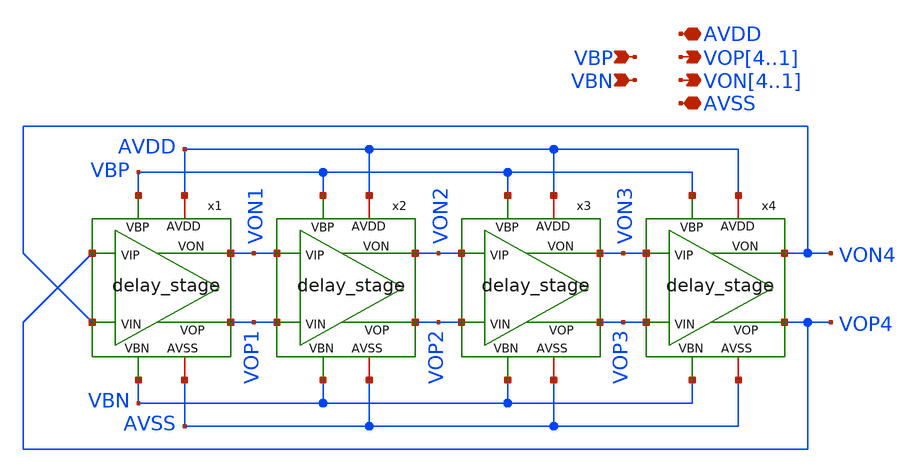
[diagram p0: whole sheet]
** sch_path: designs/libs/core_analog/vco/vco.sch
**.subckt vco VOP4,VOP3,VOP2,VOP1 VON4,VON3,VON2,VON1 VBP VBN AVDD AVSS
*.opin VOP4,VOP3,VOP2,VOP1
*.opin VON4,VON3,VON2,VON1
*.ipin VBP
*.ipin VBN
*.iopin AVDD
*.iopin AVSS
x1 VOP1 AVDD VOP4 VON4 VON1 AVSS VBP VBN delay_stage
x2 VOP2 AVDD VON1 VOP1 VON2 AVSS VBP VBN delay_stage
x3 VOP3 AVDD VON2 VOP2 VON3 AVSS VBP VBN delay_stage
x4 VOP4 AVDD VON3 VOP3 VON4 AVSS VBP VBN delay_stage
**.ends

* expanding   symbol:  libs/core_analog/delay_stage/delay_stage.sym # of pins=8
** sym_path: designs/libs/core_analog/delay_stage/delay_stage.sym
** sch_path: designs/libs/core_analog/delay_stage/delay_stage.sch
.subckt delay_stage VOP AVDD VIP VIN VON AVSS VBP VBN
*.ipin VIP
*.ipin VIN
*.opin VOP
*.opin VON
*.iopin AVDD
*.iopin AVSS
*.ipin VBP
*.ipin VBN
XM5 VON VIP net1 AVSS nfet_03v3 L=0.5u W=2.08u nf=1 ad='int((nf+1)/2) * W/nf * 0.18u' as='int((nf+2)/2) * W/nf * 0.18u'
+ pd='2*int((nf+1)/2) * (W/nf + 0.18u)' ps='2*int((nf+2)/2) * (W/nf + 0.18u)' nrd='0.18u / W' nrs='0.18u / W'
+ sa=0 sb=0 sd=0 m=8
XM2 VON VON AVDD AVDD pfet_03v3 L=1.5u W=1.1u nf=1 ad='int((nf+1)/2) * W/nf * 0.18u' as='int((nf+2)/2) * W/nf * 0.18u'
+ pd='2*int((nf+1)/2) * (W/nf + 0.18u)' ps='2*int((nf+2)/2) * (W/nf + 0.18u)' nrd='0.18u / W' nrs='0.18u / W'
+ sa=0 sb=0 sd=0 m=8
XM6 VOP VIN net1 AVSS nfet_03v3 L=0.5u W=2.08u nf=1 ad='int((nf+1)/2) * W/nf * 0.18u' as='int((nf+2)/2) * W/nf * 0.18u'
+ pd='2*int((nf+1)/2) * (W/nf + 0.18u)' ps='2*int((nf+2)/2) * (W/nf + 0.18u)' nrd='0.18u / W' nrs='0.18u / W'
+ sa=0 sb=0 sd=0 m=8
XM1 VON VBP AVDD AVDD pfet_03v3 L=1.5u W=1.1u nf=1 ad='int((nf+1)/2) * W/nf * 0.18u' as='int((nf+2)/2) * W/nf * 0.18u'
+ pd='2*int((nf+1)/2) * (W/nf + 0.18u)' ps='2*int((nf+2)/2) * (W/nf + 0.18u)' nrd='0.18u / W' nrs='0.18u / W'
+ sa=0 sb=0 sd=0 m=8
XM3 VOP VBP AVDD AVDD pfet_03v3 L=1.5u W=1.1u nf=1 ad='int((nf+1)/2) * W/nf * 0.18u' as='int((nf+2)/2) * W/nf * 0.18u'
+ pd='2*int((nf+1)/2) * (W/nf + 0.18u)' ps='2*int((nf+2)/2) * (W/nf + 0.18u)' nrd='0.18u / W' nrs='0.18u / W'
+ sa=0 sb=0 sd=0 m=8
XM4 VOP VOP AVDD AVDD pfet_03v3 L=1.5u W=1.1u nf=1 ad='int((nf+1)/2) * W/nf * 0.18u' as='int((nf+2)/2) * W/nf * 0.18u'
+ pd='2*int((nf+1)/2) * (W/nf + 0.18u)' ps='2*int((nf+2)/2) * (W/nf + 0.18u)' nrd='0.18u / W' nrs='0.18u / W'
+ sa=0 sb=0 sd=0 m=8
XM8 net1 VBN AVSS AVSS nfet_03v3 L=0.5u W=11.25u nf=1 ad='int((nf+1)/2) * W/nf * 0.18u' as='int((nf+2)/2) * W/nf * 0.18u'
+ pd='2*int((nf+1)/2) * (W/nf + 0.18u)' ps='2*int((nf+2)/2) * (W/nf + 0.18u)' nrd='0.18u / W' nrs='0.18u / W'
+ sa=0 sb=0 sd=0 m=8
.ends

.end
